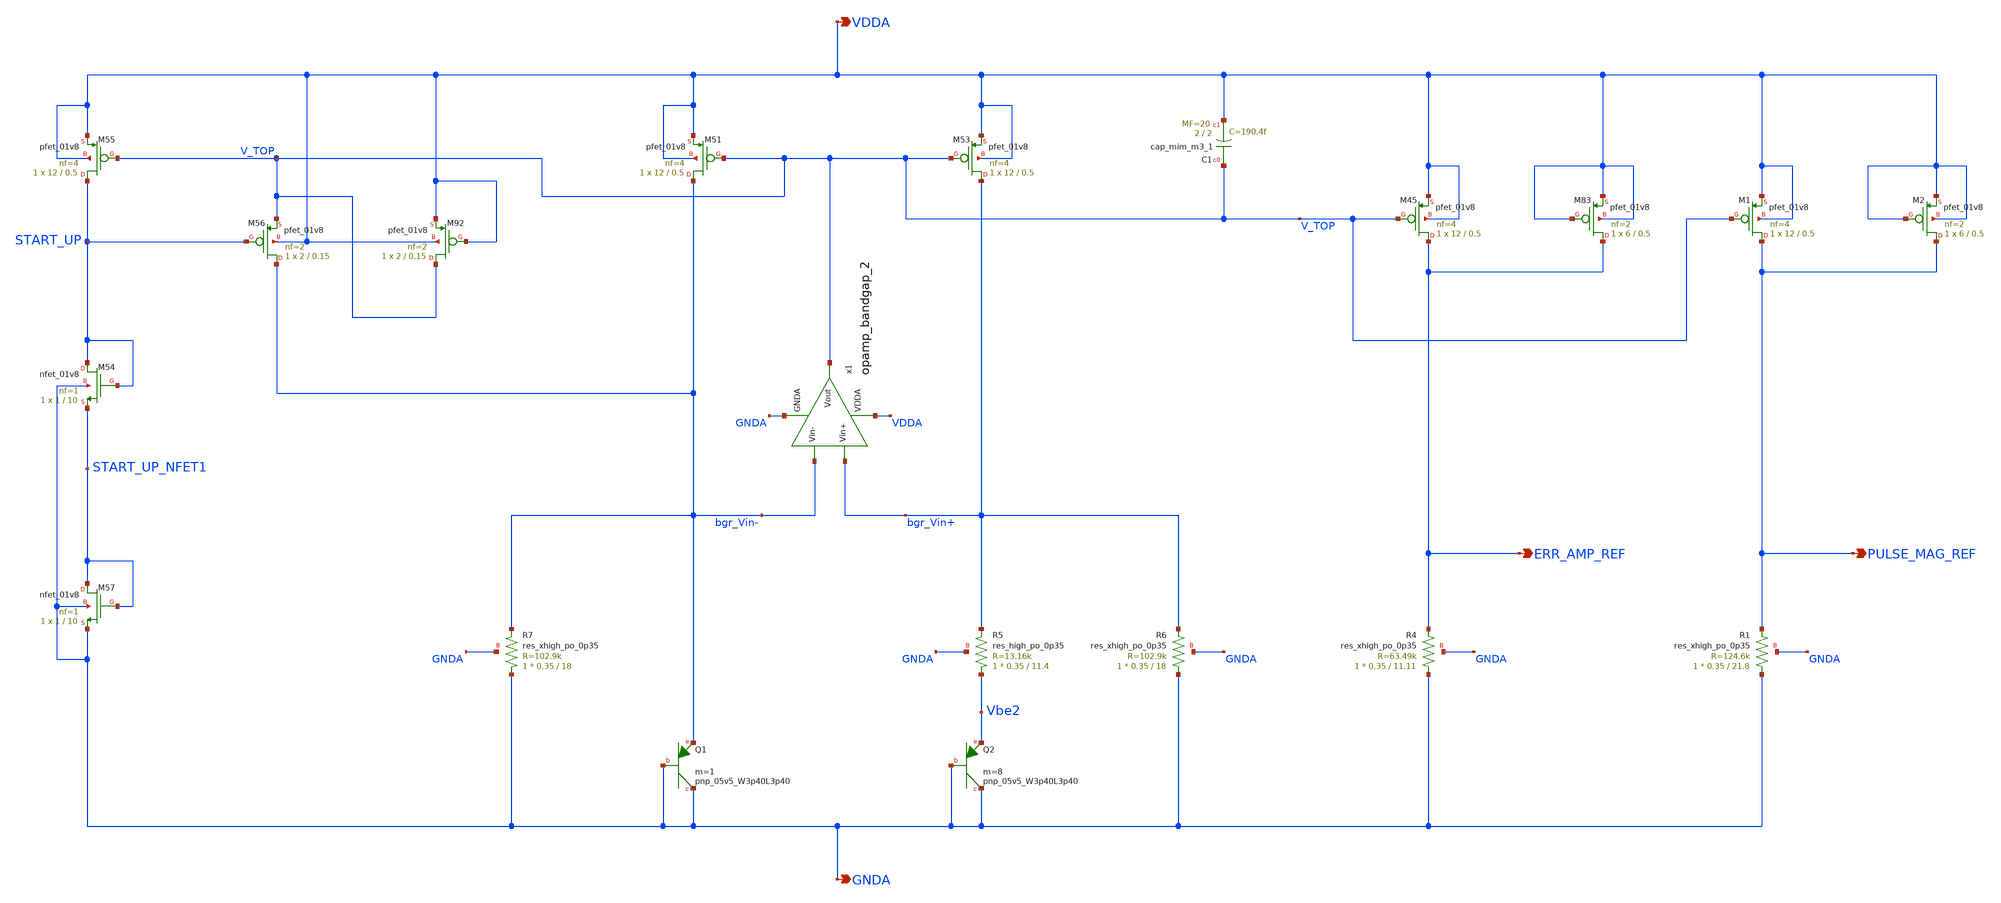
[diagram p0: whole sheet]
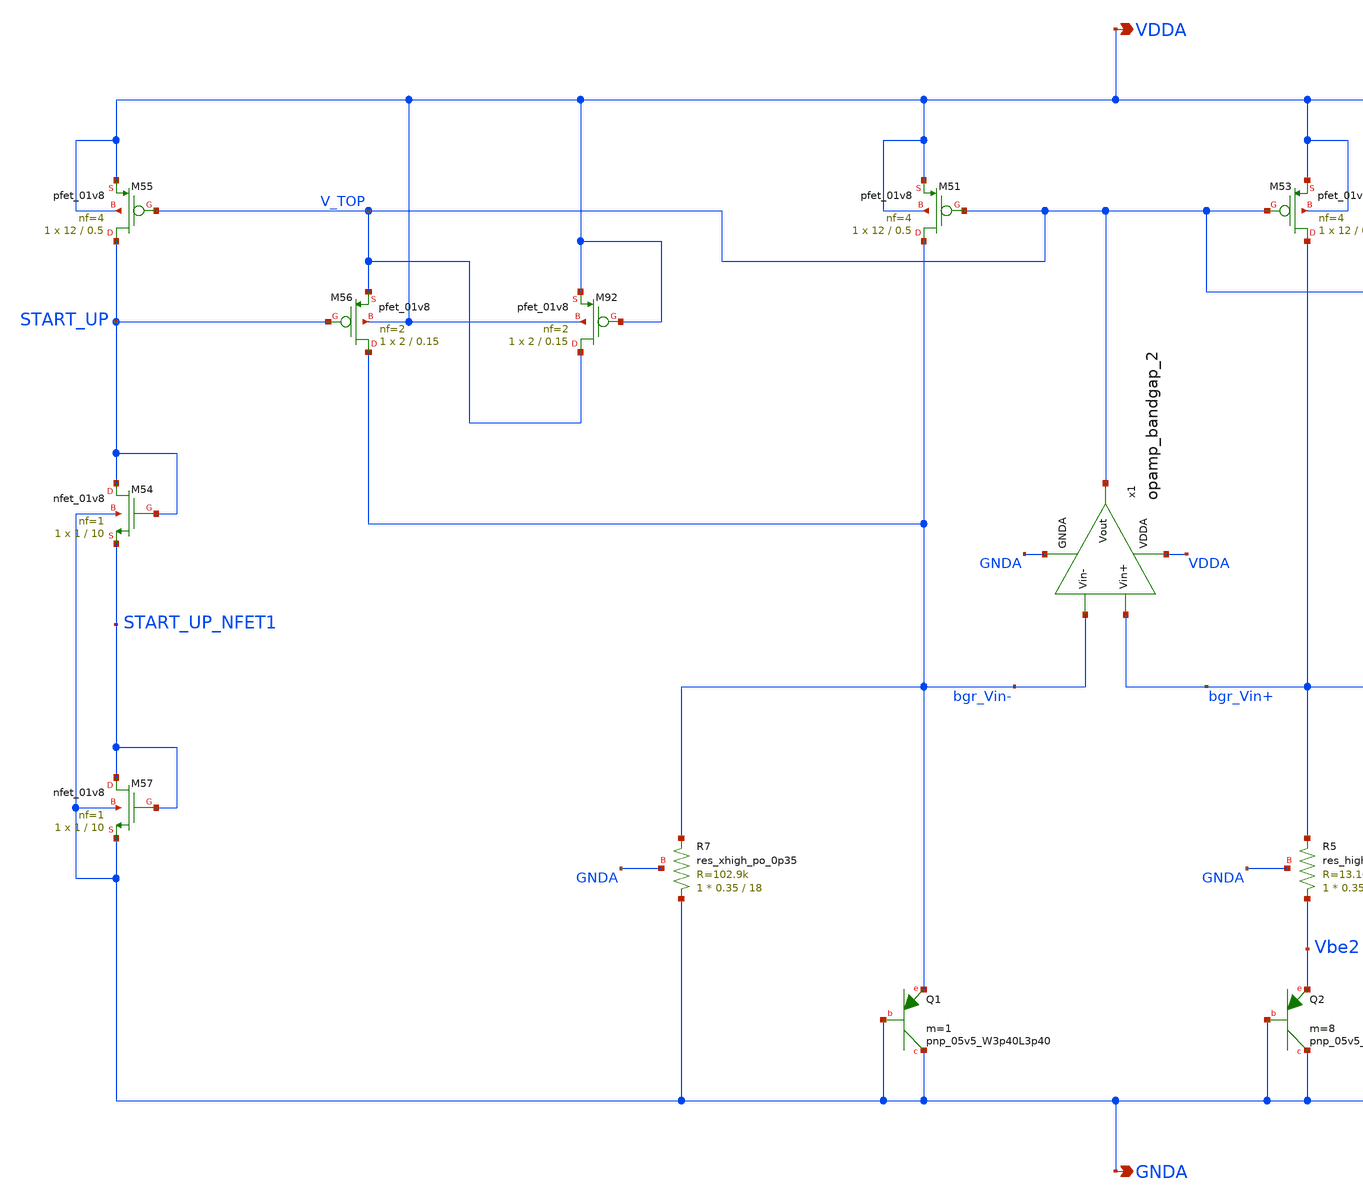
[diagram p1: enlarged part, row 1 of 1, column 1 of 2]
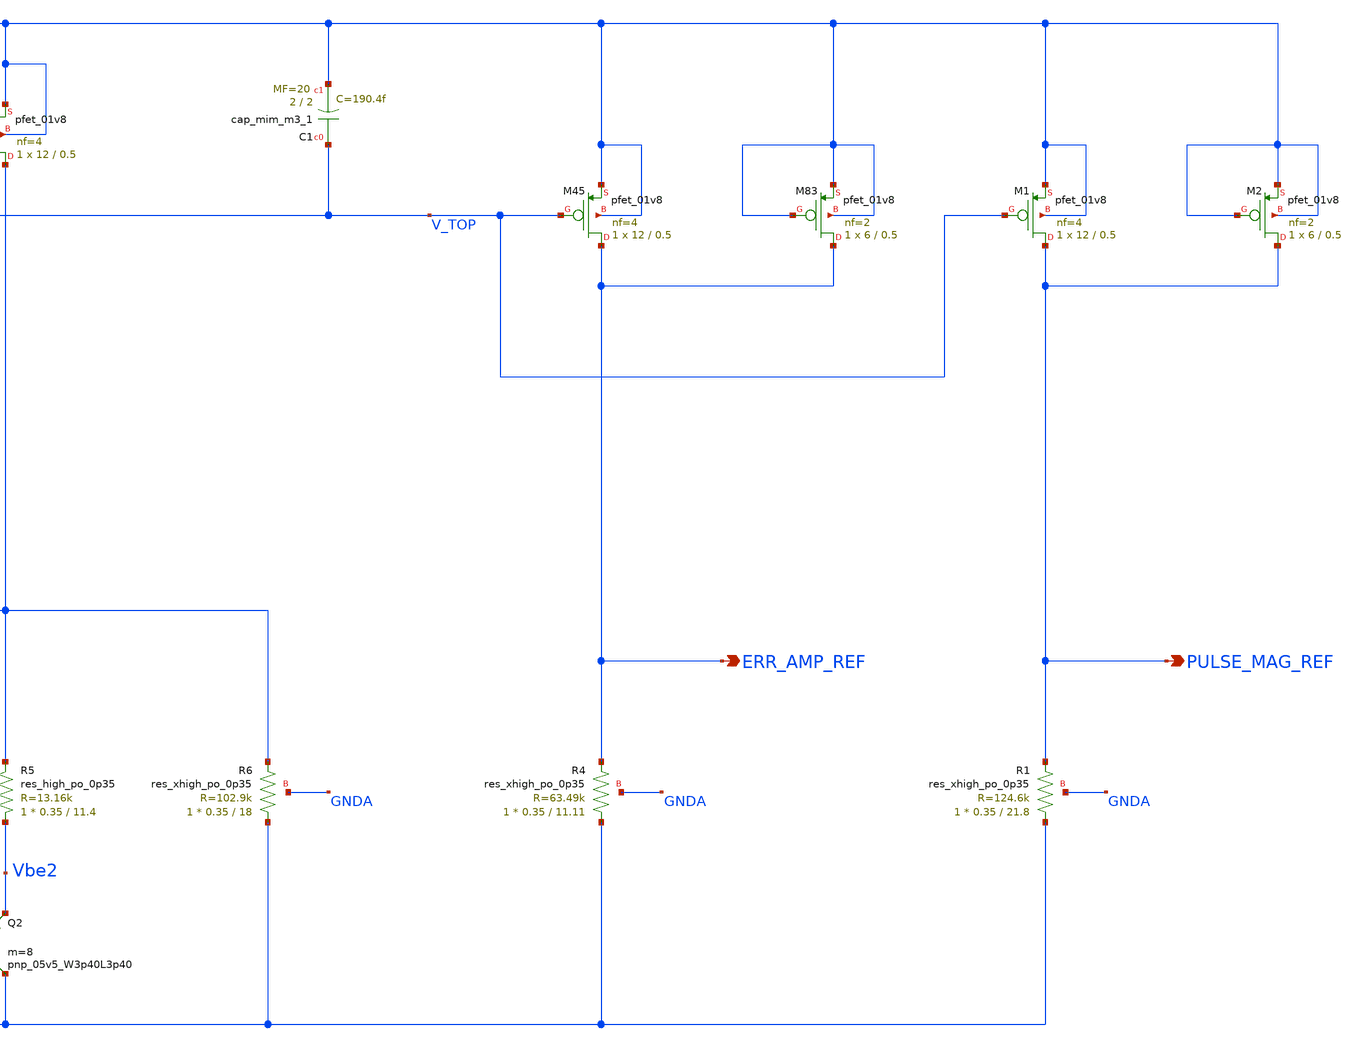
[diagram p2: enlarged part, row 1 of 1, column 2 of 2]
** sch_path: projects/ASU/EEE572/schematic/bgr_ref_volt.sch
**.subckt bgr_ref_volt VDDA GNDA ERR_AMP_REF PULSE_MAG_REF
*.opin VDDA
*.opin GNDA
*.opin ERR_AMP_REF
*.opin PULSE_MAG_REF
XM45 ERR_AMP_REF V_TOP VDDA VDDA sky130_fd_pr__pfet_01v8 L=0.5 W=12 nf=4 ad='int((nf+1)/2) * W/nf * 0.29'
+ as='int((nf+2)/2) * W/nf * 0.29' pd='2*int((nf+1)/2) * (W/nf + 0.29)' ps='2*int((nf+2)/2) * (W/nf + 0.29)'
+ nrd='0.29 / W' nrs='0.29 / W' sa=0 sb=0 sd=0 mult=1 m=1
XR4 GNDA ERR_AMP_REF GNDA sky130_fd_pr__res_xhigh_po_0p35 L=11.11 mult=1 m=1
XC1 V_TOP VDDA sky130_fd_pr__cap_mim_m3_1 W=2 L=2 MF=20 m=20
XQ1 GNDA GNDA bgr_Vin- sky130_fd_pr__pnp_05v5_W3p40L3p40 m=1
XQ2 GNDA GNDA Vbe2 sky130_fd_pr__pnp_05v5_W3p40L3p40 m=8
XM51 bgr_Vin- V_TOP VDDA VDDA sky130_fd_pr__pfet_01v8 L=0.5 W=12 nf=4 ad='int((nf+1)/2) * W/nf * 0.29'
+ as='int((nf+2)/2) * W/nf * 0.29' pd='2*int((nf+1)/2) * (W/nf + 0.29)' ps='2*int((nf+2)/2) * (W/nf + 0.29)'
+ nrd='0.29 / W' nrs='0.29 / W' sa=0 sb=0 sd=0 mult=1 m=1
XM53 bgr_Vin+ V_TOP VDDA VDDA sky130_fd_pr__pfet_01v8 L=0.5 W=12 nf=4 ad='int((nf+1)/2) * W/nf * 0.29'
+ as='int((nf+2)/2) * W/nf * 0.29' pd='2*int((nf+1)/2) * (W/nf + 0.29)' ps='2*int((nf+2)/2) * (W/nf + 0.29)'
+ nrd='0.29 / W' nrs='0.29 / W' sa=0 sb=0 sd=0 mult=1 m=1
XR6 GNDA bgr_Vin+ GNDA sky130_fd_pr__res_xhigh_po_0p35 L=18 mult=1 m=1
XR7 GNDA bgr_Vin- GNDA sky130_fd_pr__res_xhigh_po_0p35 L=18 mult=1 m=1
XM54 START_UP START_UP START_UP_NFET1 GNDA sky130_fd_pr__nfet_01v8 L=10 W=1 nf=1 ad='int((nf+1)/2) * W/nf * 0.29'
+ as='int((nf+2)/2) * W/nf * 0.29' pd='2*int((nf+1)/2) * (W/nf + 0.29)' ps='2*int((nf+2)/2) * (W/nf + 0.29)'
+ nrd='0.29 / W' nrs='0.29 / W' sa=0 sb=0 sd=0 mult=1 m=1
XM55 START_UP V_TOP VDDA VDDA sky130_fd_pr__pfet_01v8 L=0.5 W=12 nf=4 ad='int((nf+1)/2) * W/nf * 0.29'
+ as='int((nf+2)/2) * W/nf * 0.29' pd='2*int((nf+1)/2) * (W/nf + 0.29)' ps='2*int((nf+2)/2) * (W/nf + 0.29)'
+ nrd='0.29 / W' nrs='0.29 / W' sa=0 sb=0 sd=0 mult=1 m=1
XM56 bgr_Vin- START_UP V_TOP VDDA sky130_fd_pr__pfet_01v8 L=0.15 W=2 nf=2 ad='int((nf+1)/2) * W/nf * 0.29'
+ as='int((nf+2)/2) * W/nf * 0.29' pd='2*int((nf+1)/2) * (W/nf + 0.29)' ps='2*int((nf+2)/2) * (W/nf + 0.29)'
+ nrd='0.29 / W' nrs='0.29 / W' sa=0 sb=0 sd=0 mult=1 m=1
XM57 START_UP_NFET1 START_UP_NFET1 GNDA GNDA sky130_fd_pr__nfet_01v8 L=10 W=1 nf=1 ad='int((nf+1)/2) * W/nf * 0.29'
+ as='int((nf+2)/2) * W/nf * 0.29' pd='2*int((nf+1)/2) * (W/nf + 0.29)' ps='2*int((nf+2)/2) * (W/nf + 0.29)'
+ nrd='0.29 / W' nrs='0.29 / W' sa=0 sb=0 sd=0 mult=1 m=1
x1 VDDA V_TOP bgr_Vin- bgr_Vin+ GNDA opamp_bandgap_2
XM83 ERR_AMP_REF VDDA VDDA VDDA sky130_fd_pr__pfet_01v8 L=0.5 W=6 nf=2 ad='int((nf+1)/2) * W/nf * 0.29'
+ as='int((nf+2)/2) * W/nf * 0.29' pd='2*int((nf+1)/2) * (W/nf + 0.29)' ps='2*int((nf+2)/2) * (W/nf + 0.29)'
+ nrd='0.29 / W' nrs='0.29 / W' sa=0 sb=0 sd=0 mult=1 m=1
XM92 V_TOP VDDA VDDA VDDA sky130_fd_pr__pfet_01v8 L=0.15 W=2 nf=2 ad='int((nf+1)/2) * W/nf * 0.29' as='int((nf+2)/2) * W/nf * 0.29'
+ pd='2*int((nf+1)/2) * (W/nf + 0.29)' ps='2*int((nf+2)/2) * (W/nf + 0.29)' nrd='0.29 / W' nrs='0.29 / W'
+ sa=0 sb=0 sd=0 mult=1 m=1
XR5 Vbe2 bgr_Vin+ GNDA sky130_fd_pr__res_high_po_0p35 L=11.4 mult=1 m=1
XM1 PULSE_MAG_REF V_TOP VDDA VDDA sky130_fd_pr__pfet_01v8 L=0.5 W=12 nf=4 ad='int((nf+1)/2) * W/nf * 0.29'
+ as='int((nf+2)/2) * W/nf * 0.29' pd='2*int((nf+1)/2) * (W/nf + 0.29)' ps='2*int((nf+2)/2) * (W/nf + 0.29)'
+ nrd='0.29 / W' nrs='0.29 / W' sa=0 sb=0 sd=0 mult=1 m=1
XR1 GNDA PULSE_MAG_REF GNDA sky130_fd_pr__res_xhigh_po_0p35 L=21.8 mult=1 m=1
XM2 PULSE_MAG_REF VDDA VDDA VDDA sky130_fd_pr__pfet_01v8 L=0.5 W=6 nf=2 ad='int((nf+1)/2) * W/nf * 0.29'
+ as='int((nf+2)/2) * W/nf * 0.29' pd='2*int((nf+1)/2) * (W/nf + 0.29)' ps='2*int((nf+2)/2) * (W/nf + 0.29)'
+ nrd='0.29 / W' nrs='0.29 / W' sa=0 sb=0 sd=0 mult=1 m=1
**.ends

* expanding   symbol:
*+  /foss/designs/my_design/projects/bandgapref/xschem_ngspice/new_files/opamp_bandgap_2.sym # of pins=5
** sym_path: projects/bandgapref/xschem_ngspice/new_files/opamp_bandgap_2.sym
** sch_path: projects/bandgapref/xschem_ngspice/new_files/opamp_bandgap_2.sch
.subckt opamp_bandgap_2 VDDA Vout Vin- Vin+ GNDA
*.ipin Vin+
*.opin Vout
*.ipin Vin-
*.ipin GNDA
*.ipin VDDA
XM1 V_p VDDA GNDA GNDA sky130_fd_pr__nfet_01v8 L=10 W=5 nf=1 ad='int((nf+1)/2) * W/nf * 0.29' as='int((nf+2)/2) * W/nf * 0.29'
+ pd='2*int((nf+1)/2) * (W/nf + 0.29)' ps='2*int((nf+2)/2) * (W/nf + 0.29)' nrd='0.29 / W' nrs='0.29 / W'
+ sa=0 sb=0 sd=0 mult=1 m=1
XM2 V_mirror Vin- V_p GNDA sky130_fd_pr__nfet_01v8 L=0.2 W=5 nf=1 ad='int((nf+1)/2) * W/nf * 0.29' as='int((nf+2)/2) * W/nf * 0.29'
+ pd='2*int((nf+1)/2) * (W/nf + 0.29)' ps='2*int((nf+2)/2) * (W/nf + 0.29)' nrd='0.29 / W' nrs='0.29 / W'
+ sa=0 sb=0 sd=0 mult=1 m=1
XM3 1st_Vout Vin+ V_p GNDA sky130_fd_pr__nfet_01v8 L=0.2 W=5 nf=1 ad='int((nf+1)/2) * W/nf * 0.29' as='int((nf+2)/2) * W/nf * 0.29'
+ pd='2*int((nf+1)/2) * (W/nf + 0.29)' ps='2*int((nf+2)/2) * (W/nf + 0.29)' nrd='0.29 / W' nrs='0.29 / W'
+ sa=0 sb=0 sd=0 mult=1 m=1
XM5 V_mirror V_mirror VDDA VDDA sky130_fd_pr__pfet_01v8 L=0.2 W=10 nf=2 ad='int((nf+1)/2) * W/nf * 0.29'
+ as='int((nf+2)/2) * W/nf * 0.29' pd='2*int((nf+1)/2) * (W/nf + 0.29)' ps='2*int((nf+2)/2) * (W/nf + 0.29)'
+ nrd='0.29 / W' nrs='0.29 / W' sa=0 sb=0 sd=0 mult=1 m=1
XM6 1st_Vout V_mirror VDDA VDDA sky130_fd_pr__pfet_01v8 L=0.2 W=10 nf=2 ad='int((nf+1)/2) * W/nf * 0.29'
+ as='int((nf+2)/2) * W/nf * 0.29' pd='2*int((nf+1)/2) * (W/nf + 0.29)' ps='2*int((nf+2)/2) * (W/nf + 0.29)'
+ nrd='0.29 / W' nrs='0.29 / W' sa=0 sb=0 sd=0 mult=1 m=1
XM4 Vout VDDA GNDA GNDA sky130_fd_pr__nfet_01v8 L=10 W=5 nf=1 ad='int((nf+1)/2) * W/nf * 0.29' as='int((nf+2)/2) * W/nf * 0.29'
+ pd='2*int((nf+1)/2) * (W/nf + 0.29)' ps='2*int((nf+2)/2) * (W/nf + 0.29)' nrd='0.29 / W' nrs='0.29 / W'
+ sa=0 sb=0 sd=0 mult=1 m=1
XM7 Vout 1st_Vout VDDA VDDA sky130_fd_pr__pfet_01v8 L=0.2 W=10 nf=2 ad='int((nf+1)/2) * W/nf * 0.29'
+ as='int((nf+2)/2) * W/nf * 0.29' pd='2*int((nf+1)/2) * (W/nf + 0.29)' ps='2*int((nf+2)/2) * (W/nf + 0.29)'
+ nrd='0.29 / W' nrs='0.29 / W' sa=0 sb=0 sd=0 mult=1 m=1
.ends

.end
